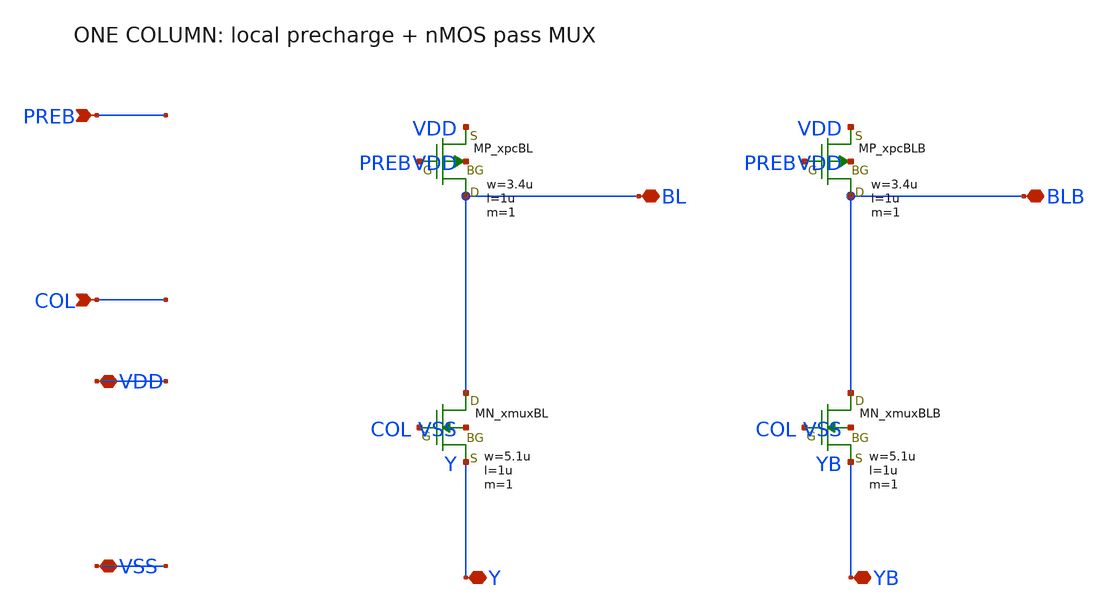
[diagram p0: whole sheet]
** sch_path: member_project/SRAM/PenguinEino/sram512/schematics/sram512_column.sch
**.subckt sram512_column BL Y BLB YB PREB COL VDD VSS
*.iopin BL
*.iopin Y
*.iopin BLB
*.iopin YB
*.ipin PREB
*.ipin COL
*.iopin VDD
*.iopin VSS
XxpcBL BL PREB VDD VDD PMOS w=3.4u l=1u nrd=0 nrs=0 m=1
XxmuxBL BL COL Y VSS NMOS w=5.1u l=1u nrd=0 nrs=0 m=1
XxpcBLB BLB PREB VDD VDD PMOS w=3.4u l=1u nrd=0 nrs=0 m=1
XxmuxBLB BLB COL YB VSS NMOS w=5.1u l=1u nrd=0 nrs=0 m=1
**.ends
.end
